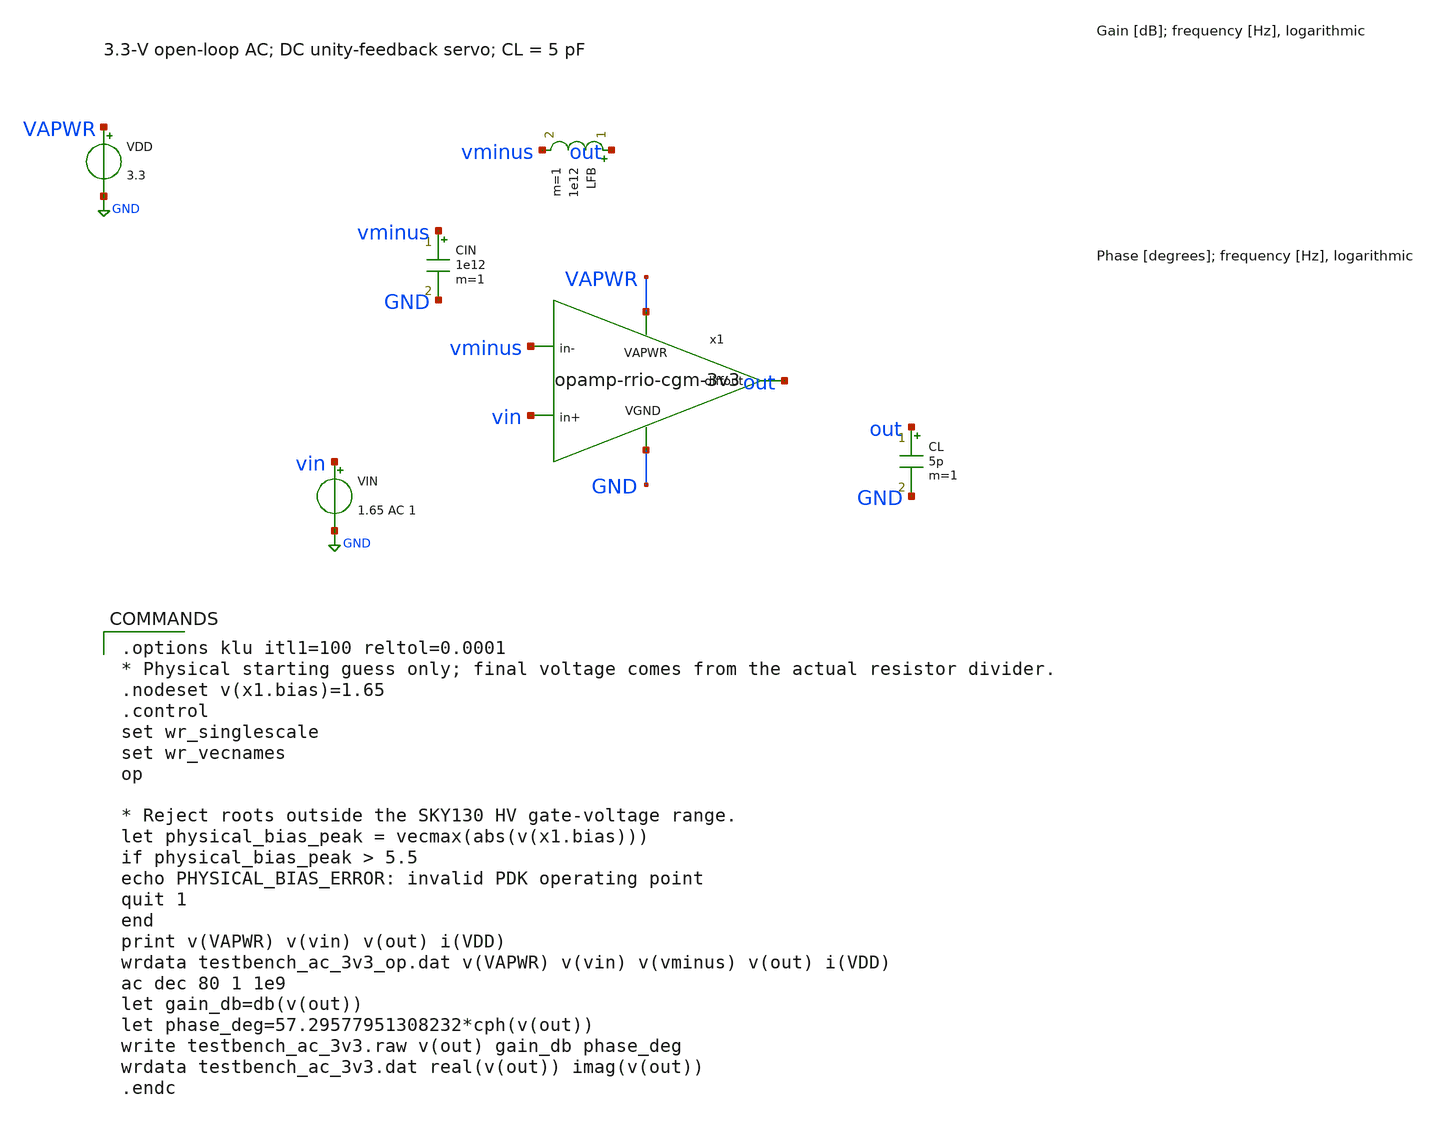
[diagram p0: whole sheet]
** sch_path: xschem/testbench_ac_3v3.sch
**.subckt testbench_ac_3v3
x1 VAPWR out vin vminus GND opamp-rrio-cgm-3v3
VDD VAPWR GND 3.3
VIN vin GND 1.65 AC 1
LFB out vminus 1e12 m=1
CIN vminus GND 1e12 m=1
CL out GND 5p m=1
**** begin user architecture code
 .lib $::SKYWATER_MODELS/sky130.lib.spice tt

.options klu itl1=100 reltol=0.0001
* Physical starting guess only; final voltage comes from the actual resistor divider.
.nodeset v(x1.bias)=1.65
.control
set wr_singlescale
set wr_vecnames
op

* Reject roots outside the SKY130 HV gate-voltage range.
let physical_bias_peak = vecmax(abs(v(x1.bias)))
if physical_bias_peak > 5.5
echo PHYSICAL_BIAS_ERROR: invalid PDK operating point
quit 1
end
print v(VAPWR) v(vin) v(out) i(VDD)
wrdata testbench_ac_3v3_op.dat v(VAPWR) v(vin) v(vminus) v(out) i(VDD)
ac dec 80 1 1e9
let gain_db=db(v(out))
let phase_deg=57.29577951308232*cph(v(out))
write testbench_ac_3v3.raw v(out) gain_db phase_deg
wrdata testbench_ac_3v3.dat real(v(out)) imag(v(out))
.endc

**** end user architecture code
**.ends
.GLOBAL GND
.end
